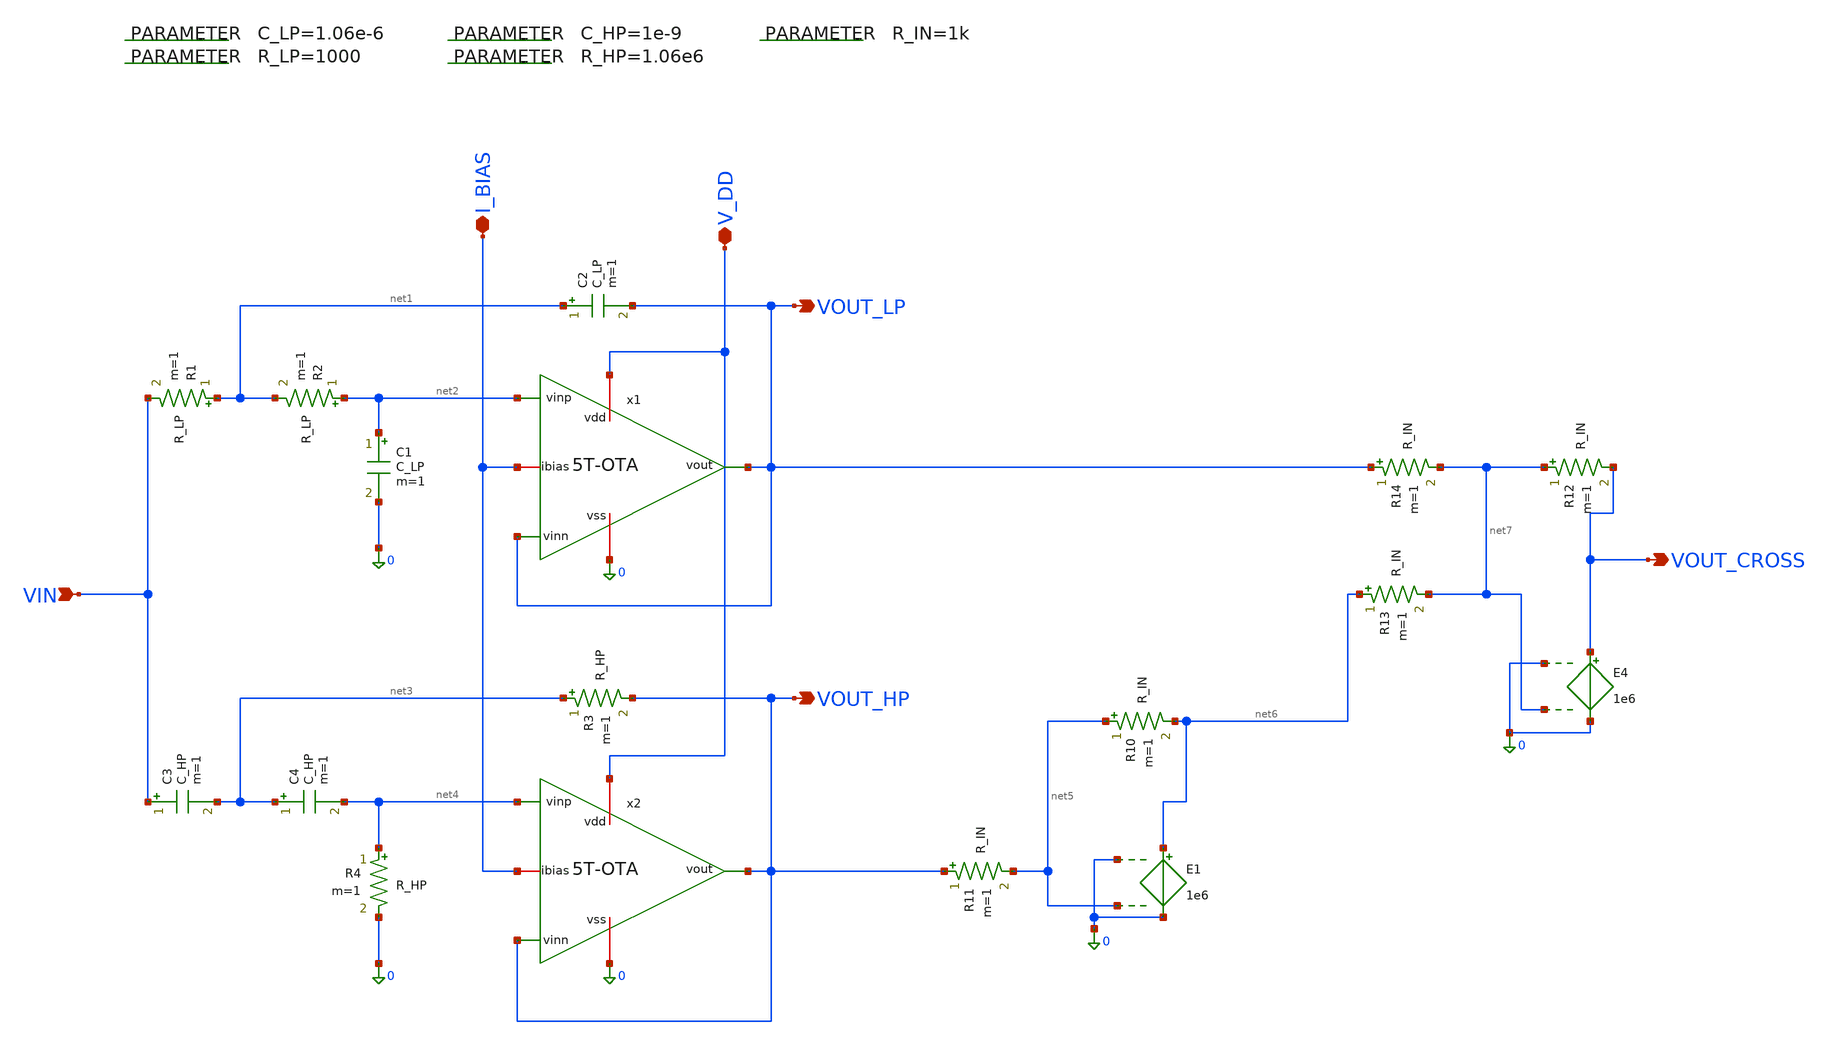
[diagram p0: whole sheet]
** sch_path: 004_Real_Circuits/linkwtz_riley_crossover_improved_OTA.sch
**.subckt linkwtz_riley_crossover_improved_OTA VOUT_LP VOUT_HP VIN I_BIAS V_DD VOUT_CROSS
*.opin VOUT_LP
*.opin VOUT_HP
*.ipin VIN
*.iopin I_BIAS
*.iopin V_DD
*.opin VOUT_CROSS
x1 V_DD VOUT_LP I_BIAS net2 VOUT_LP 0 5T-OTA
x2 V_DD VOUT_HP I_BIAS net4 VOUT_HP 0 5T-OTA
R1 net1 VIN R_LP m=1
.param C_LP=1.06e-6
.param R_LP=1000
.param C_HP=1e-9
.param R_HP=1.06e6
.param R_IN=1k
R2 net2 net1 R_LP m=1
C1 net2 0 C_LP m=1
C2 net1 VOUT_LP C_LP m=1
C3 VIN net3 C_HP m=1
C4 net3 net4 C_HP m=1
R3 net3 VOUT_HP R_HP m=1
R4 net4 0 R_HP m=1
R10 net5 net6 R_IN m=1
R11 VOUT_HP net5 R_IN m=1
R12 net7 VOUT_CROSS R_IN m=1
R13 net6 net7 R_IN m=1
R14 VOUT_LP net7 R_IN m=1
E1 net6 0 0 net5 1e6
E4 VOUT_CROSS 0 0 net7 1e6
**.ends

* expanding   symbol:  /foss/designs/Repo/004_Real_Circuits/5T-OTA.sym # of pins=6
** sym_path: 004_Real_Circuits/5T-OTA.sym
** sch_path: 004_Real_Circuits/5T-OTA.sch
.subckt 5T-OTA vdd vout ibias vinp vinn vss
*.ipin vinp
*.iopin vdd
*.iopin vss
*.opin vout
*.ipin vinn
*.iopin ibias
XM1 net3 vinp net1 net4 sg13_lv_nmos w=2u l=5u ng=1 m=1 mm_ok=1
XM5 net1 net2 vss vss sg13_lv_nmos w=0.5u l=5u ng=1 m=1 mm_ok=1
XM2 vout vinn net1 net5 sg13_lv_nmos w=2u l=5u ng=1 m=1 mm_ok=1
XM6 net2 net2 vss vss sg13_lv_nmos w=2.5u l=5u ng=1 m=1 mm_ok=1
XM3 net3 net3 vdd vdd sg13_lv_pmos w=1.5u l=5u ng=1 m=1 mm_ok=1
XM4 vout net3 vdd vdd sg13_lv_pmos w=1.5u l=5u ng=1 m=1 mm_ok=1
XM7 net2 ibias vdd net6 sg13_lv_pmos w=0.15u l=0.13u ng=1 m=1 mm_ok=1
.ends

.end
